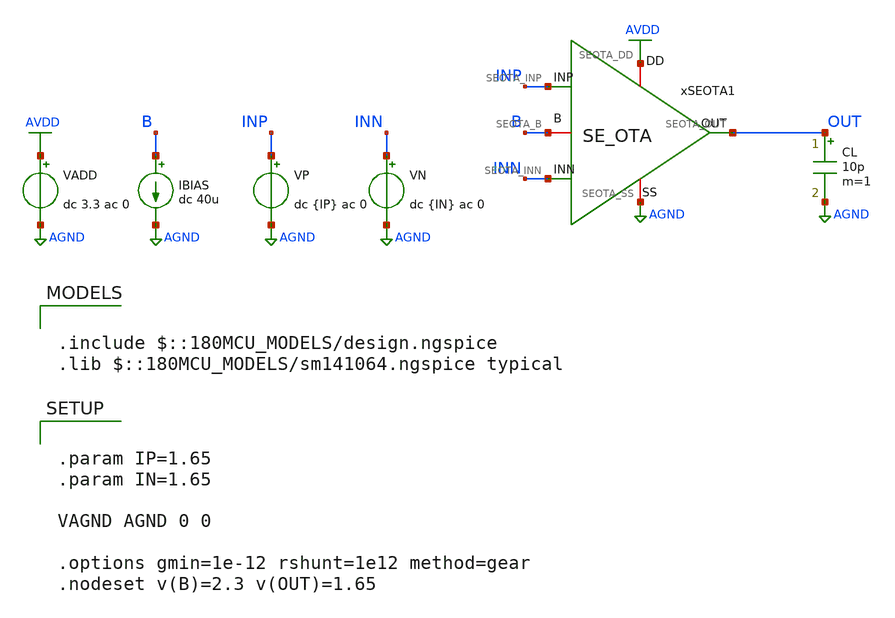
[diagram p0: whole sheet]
** sch_path: Design_Files/IC Design/Testbench/SE_OTA_OTA/SE_OTA_TB_OL.sch
**.subckt SE_OTA_TB_OL
IBIAS B AGND dc 40u
VADD AVDD AGND dc 3.3 ac 0
.save i(vadd)
CL OUT AGND 10p m=1
VP INP AGND dc {IP} ac 0
VN INN AGND dc {IN} ac 0
xSEOTA1 AVDD AGND INP INN OUT B SE_OTA
**** begin user architecture code

.include $::180MCU_MODELS/design.ngspice
.lib $::180MCU_MODELS/sm141064.ngspice typical



.control
destroy all
save all
set wr_singlescale

shell mkdir -p /foss/designs/ECG_Acquisition_IC/Measurement_Results/IC_Simulation/SE_OTA

* =========================================================
* SE_OTA_TB_OL
* Save TXT only
* =========================================================

* OP: Vin,cm, Vout,DC, B
op
wrdata /foss/designs/ECG_Acquisition_IC/Measurement_Results/IC_Simulation/SE_OTA/ol_op.txt v(INP)
+ v(INN) v(OUT) v(B)

* Input offset sweep
dc VP 1.60 1.70 0.00001
wrdata /foss/designs/ECG_Acquisition_IC/Measurement_Results/IC_Simulation/SE_OTA/ol_offset.txt
+ v(INP) v(INN) v(OUT)

* Differential AC gain
alter @VP[DC] = 1.65
alter @VN[DC] = 1.65
alter @VP[ACMAG] = 0.5
alter @VP[ACPHASE] = 0
alter @VN[ACMAG] = 0.5
alter @VN[ACPHASE] = 180
alter @VADD[ACMAG] = 0

ac dec 200 1 1G
wrdata /foss/designs/ECG_Acquisition_IC/Measurement_Results/IC_Simulation/SE_OTA/ol_ac_diff.txt
+ db(v(OUT)) ph(v(OUT)) mag(v(OUT))

* CMRR
alter @VP[ACMAG] = 1
alter @VP[ACPHASE] = 0
alter @VN[ACMAG] = 1
alter @VN[ACPHASE] = 0
alter @VADD[ACMAG] = 0

ac dec 200 1 1G
wrdata /foss/designs/ECG_Acquisition_IC/Measurement_Results/IC_Simulation/SE_OTA/ol_ac_cm.txt
+ db(v(OUT)) mag(v(OUT))

* PSRR+
alter @VP[ACMAG] = 0
alter @VN[ACMAG] = 0
alter @VADD[ACMAG] = 1
alter @VADD[ACPHASE] = 0

ac dec 200 1 1G
wrdata /foss/designs/ECG_Acquisition_IC/Measurement_Results/IC_Simulation/SE_OTA/ol_ac_psrr.txt
+ db(v(OUT)) mag(v(OUT))

* Noise total only
* Saves integrated noise from 0.05 Hz to 150 Hz
alter @VADD[ACMAG] = 0
alter @VP[ACMAG] = 1
alter @VN[ACMAG] = 0

noise v(OUT) VP dec 100 0.05 150
wrdata /foss/designs/ECG_Acquisition_IC/Measurement_Results/IC_Simulation/SE_OTA/ol_noise_total.txt
+ inoise_total onoise_total

.endc




.param IP=1.65
.param IN=1.65

VAGND AGND 0 0

.options gmin=1e-12 rshunt=1e12 method=gear
.nodeset v(B)=2.3 v(OUT)=1.65


**** end user architecture code
**.ends

* expanding   symbol:  ECG_Acquisition_IC/Design_Files/IC Design/Schematic/SE_OTA/SE_OTA.sym # of
*+ pins=6
** sym_path: Design_Files/IC Design/Schematic/SE_OTA/SE_OTA.sym
** sch_path: Design_Files/IC Design/Schematic/SE_OTA/SE_OTA.sch
.subckt SE_OTA SEOTA_DD SEOTA_SS SEOTA_INP SEOTA_INN SEOTA_OUT SEOTA_B
*.iopin SEOTA_DD
*.iopin SEOTA_SS
*.ipin SEOTA_INP
*.ipin SEOTA_INN
*.opin SEOTA_OUT
*.iopin SEOTA_B
XM4 net1 net4 SEOTA_SS SEOTA_SS nfet_03v3 L=2u W=4u nf=1 ad='int((nf+1)/2) * W/nf * 0.18u' as='int((nf+2)/2) * W/nf * 0.18u'
+ pd='2*int((nf+1)/2) * (W/nf + 0.18u)' ps='2*int((nf+2)/2) * (W/nf + 0.18u)' nrd='0.18u / W' nrs='0.18u / W'
+ sa=0 sb=0 sd=0 m=1
XM3 net4 net4 SEOTA_SS SEOTA_SS nfet_03v3 L=2u W=4u nf=1 ad='int((nf+1)/2) * W/nf * 0.18u' as='int((nf+2)/2) * W/nf * 0.18u'
+ pd='2*int((nf+1)/2) * (W/nf + 0.18u)' ps='2*int((nf+2)/2) * (W/nf + 0.18u)' nrd='0.18u / W' nrs='0.18u / W'
+ sa=0 sb=0 sd=0 m=1
XM1 net4 SEOTA_INN net3 SEOTA_DD pfet_03v3 L=1u W=4u nf=1 ad='int((nf+1)/2) * W/nf * 0.18u' as='int((nf+2)/2) * W/nf * 0.18u'
+ pd='2*int((nf+1)/2) * (W/nf + 0.18u)' ps='2*int((nf+2)/2) * (W/nf + 0.18u)' nrd='0.18u / W' nrs='0.18u / W'
+ sa=0 sb=0 sd=0 m=16
XM2 net1 SEOTA_INP net3 SEOTA_DD pfet_03v3 L=1u W=4u nf=1 ad='int((nf+1)/2) * W/nf * 0.18u' as='int((nf+2)/2) * W/nf * 0.18u'
+ pd='2*int((nf+1)/2) * (W/nf + 0.18u)' ps='2*int((nf+2)/2) * (W/nf + 0.18u)' nrd='0.18u / W' nrs='0.18u / W'
+ sa=0 sb=0 sd=0 m=16
XM7 SEOTA_OUT SEOTA_B SEOTA_DD SEOTA_DD pfet_03v3 L=0.5u W=4u nf=1 ad='int((nf+1)/2) * W/nf * 0.18u'
+ as='int((nf+2)/2) * W/nf * 0.18u' pd='2*int((nf+1)/2) * (W/nf + 0.18u)' ps='2*int((nf+2)/2) * (W/nf + 0.18u)'
+ nrd='0.18u / W' nrs='0.18u / W' sa=0 sb=0 sd=0 m=28
Rz net1 net2 0.5k m=1
XM5 net3 SEOTA_B SEOTA_DD SEOTA_DD pfet_03v3 L=2u W=4u nf=1 ad='int((nf+1)/2) * W/nf * 0.18u' as='int((nf+2)/2) * W/nf * 0.18u'
+ pd='2*int((nf+1)/2) * (W/nf + 0.18u)' ps='2*int((nf+2)/2) * (W/nf + 0.18u)' nrd='0.18u / W' nrs='0.18u / W'
+ sa=0 sb=0 sd=0 m=10
XM6 SEOTA_OUT net1 SEOTA_SS SEOTA_SS nfet_03v3 L=0.5u W=4u nf=1 ad='int((nf+1)/2) * W/nf * 0.18u' as='int((nf+2)/2) * W/nf * 0.18u'
+ pd='2*int((nf+1)/2) * (W/nf + 0.18u)' ps='2*int((nf+2)/2) * (W/nf + 0.18u)' nrd='0.18u / W' nrs='0.18u / W'
+ sa=0 sb=0 sd=0 m=8
XM8 SEOTA_B SEOTA_B SEOTA_DD SEOTA_DD pfet_03v3 L=2u W=4u nf=1 ad='int((nf+1)/2) * W/nf * 0.18u' as='int((nf+2)/2) * W/nf * 0.18u'
+ pd='2*int((nf+1)/2) * (W/nf + 0.18u)' ps='2*int((nf+2)/2) * (W/nf + 0.18u)' nrd='0.18u / W' nrs='0.18u / W'
+ sa=0 sb=0 sd=0 m=25
Cc net2 SEOTA_OUT 2p m=1
.ends

.GLOBAL AVDD
.GLOBAL AGND
.end
